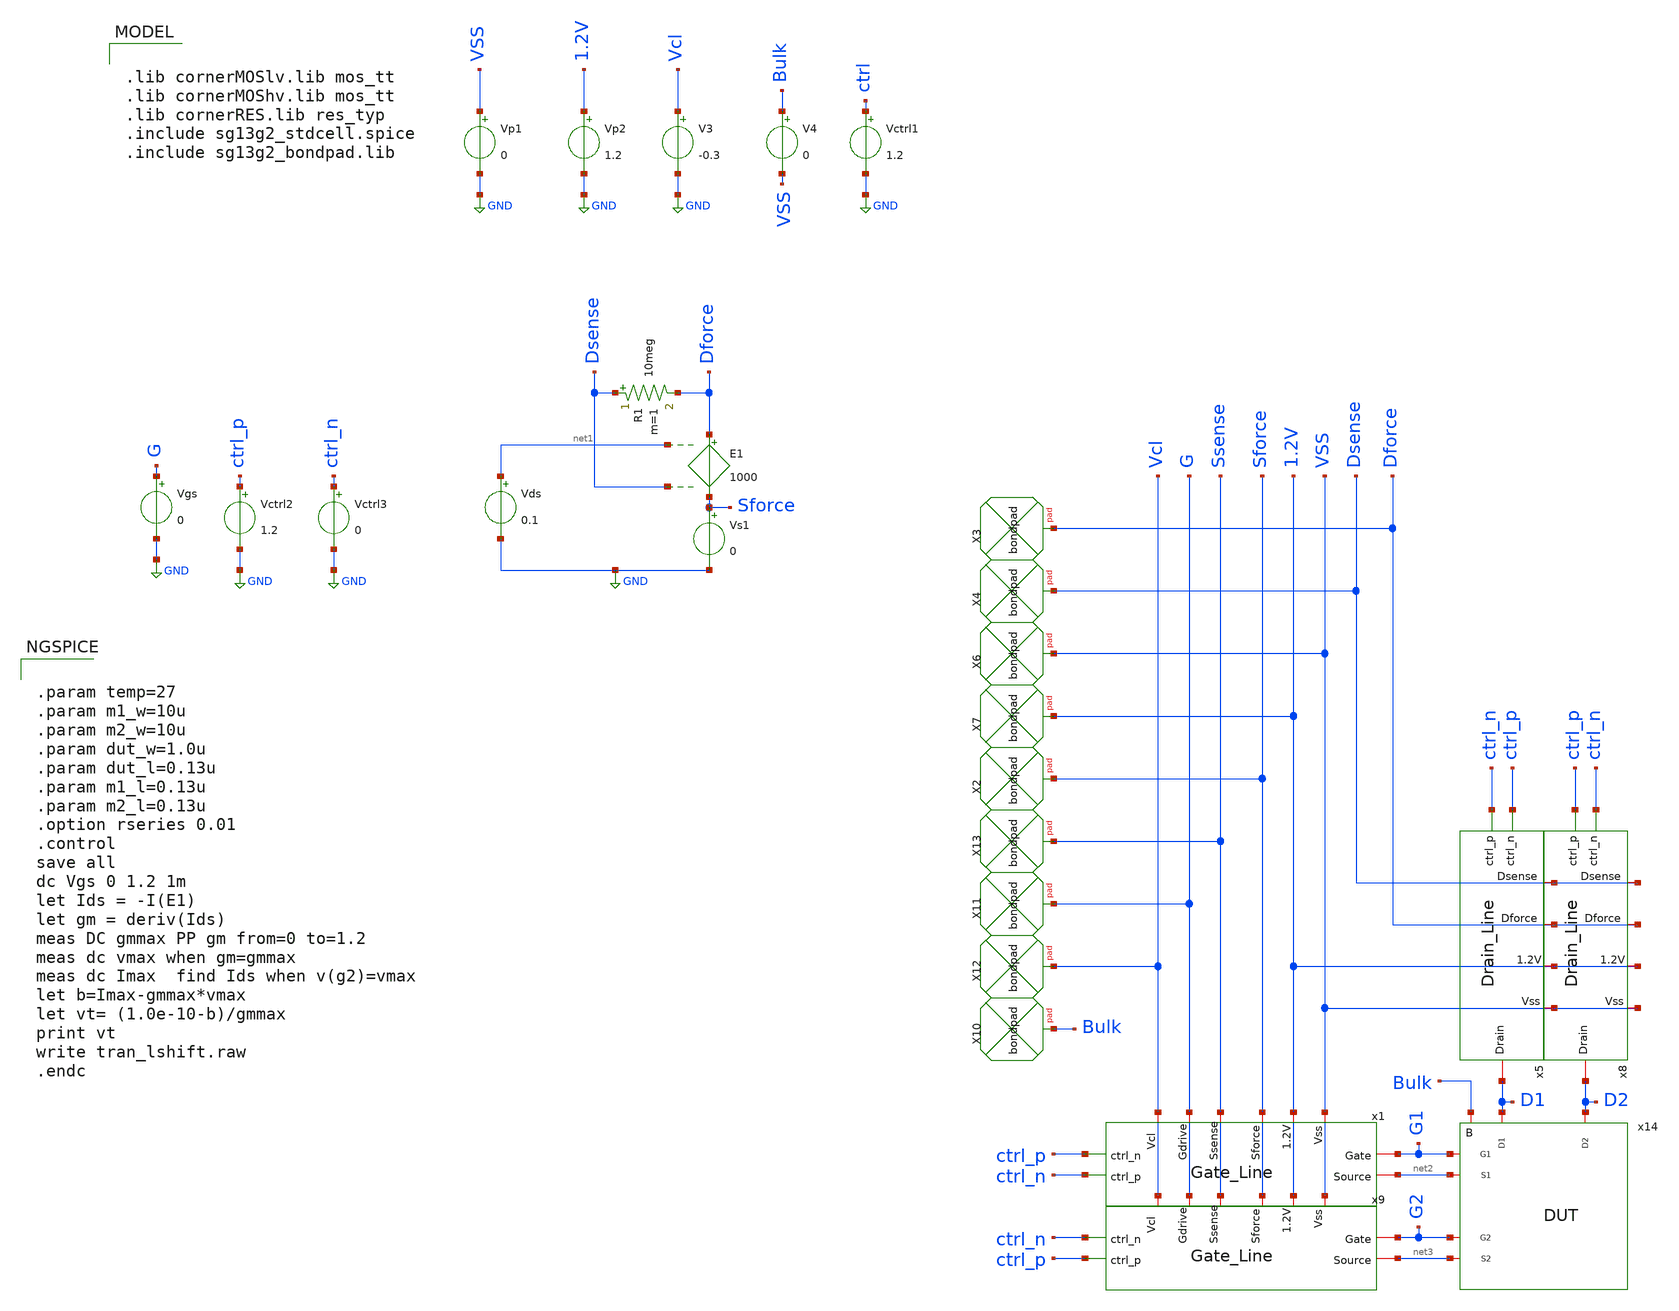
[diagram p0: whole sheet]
** sch_path: design_data/xschem/new_tb/MissMatch_chip_tb.sch
**.subckt MissMatch_chip_tb
Vp2 1.2V GND 1.2
V3 Vcl GND -0.3
XX2 Sforce bondpad size=80u shape=0 padtype=0
XX3 Dforce bondpad size=80u shape=0 padtype=0
XX4 Dsense bondpad size=80u shape=0 padtype=0
XX6 VSS bondpad size=80u shape=0 padtype=0
XX7 1.2V bondpad size=80u shape=0 padtype=0
Vp1 VSS GND 0
XX10 Bulk bondpad size=80u shape=0 padtype=0
V4 Bulk VSS 0
Vs1 Sforce GND 0
E1 Dforce Sforce net1 Dsense 1000
Vds net1 GND 0.1
R1 Dsense Dforce 10meg m=1
Vctrl1 ctrl GND 1.2
Vgs G GND 0
Vctrl2 ctrl_p GND 1.2
Vctrl3 ctrl_n GND 0
XX13 Ssense bondpad size=80u shape=0 padtype=0
XX11 G bondpad size=80u shape=0 padtype=0
XX12 Vcl bondpad size=80u shape=0 padtype=0
x1 ctrl_p ctrl_n Vcl G Ssense Sforce 1.2V VSS net2 G1 Gate_Line
x9 ctrl_n ctrl_p Vcl G Ssense Sforce 1.2V VSS net3 G2 Gate_Line
x14 Bulk D1 D2 G1 net2 G2 net3 DUT
x5 ctrl_p ctrl_n Dsense Dforce 1.2V D1 VSS Drain_Line
x8 ctrl_n ctrl_p Dsense Dforce 1.2V D2 VSS Drain_Line
**** begin user architecture code

.lib cornerMOSlv.lib mos_tt
.lib cornerMOShv.lib mos_tt
.lib cornerRES.lib res_typ
.include sg13g2_stdcell.spice
.include sg13g2_bondpad.lib



.param temp=27
.param m1_w=10u
.param m2_w=10u
.param dut_w=1.0u
.param dut_l=0.13u
.param m1_l=0.13u
.param m2_l=0.13u
.option rseries 0.01
.control
save all
dc Vgs 0 1.2 1m
let Ids = -I(E1)
let gm = deriv(Ids)
meas DC gmmax PP gm from=0 to=1.2
meas dc vmax when gm=gmmax
meas dc Imax  find Ids when v(g2)=vmax
let b=Imax-gmmax*vmax
let vt= (1.0e-10-b)/gmmax
print vt
write tran_lshift.raw
.endc


**** end user architecture code
**.ends
.GLOBAL GND
.end
